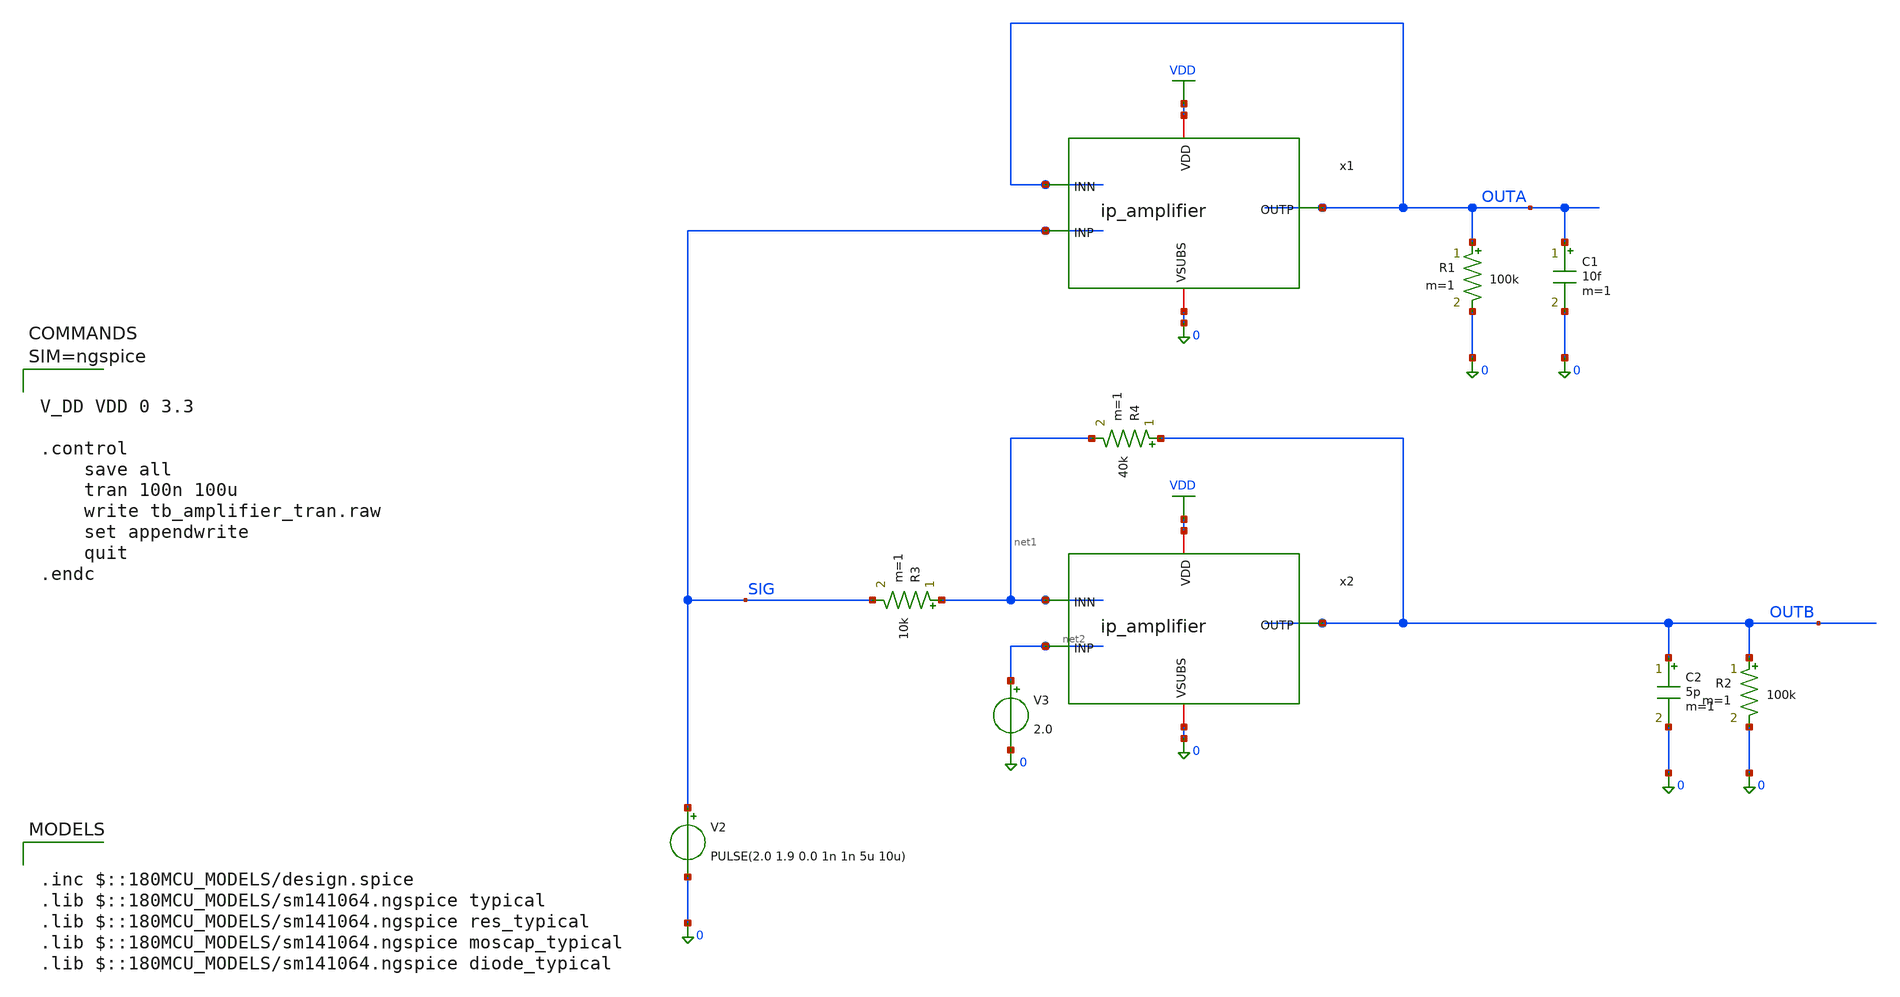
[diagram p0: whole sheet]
** sch_path: xschem/tb_amplifier_tran.sch
**.subckt tb_amplifier_tran
V2 SIG 0 PULSE(2.0 1.9 0.0 1n 1n 5u 10u)
x2 VDD OUTB net2 net1 0 ip_amplifier
R2 OUTB 0 100k m=1
C2 OUTB 0 5p m=1
V3 net2 0 2.0
R3 net1 SIG 10k m=1
R4 OUTB net1 40k m=1
x1 VDD OUTA SIG OUTA 0 ip_amplifier
R1 OUTA 0 100k m=1
C1 OUTA 0 10f m=1
**** begin user architecture code

.inc $::180MCU_MODELS/design.spice
.lib $::180MCU_MODELS/sm141064.ngspice typical
.lib $::180MCU_MODELS/sm141064.ngspice res_typical
.lib $::180MCU_MODELS/sm141064.ngspice moscap_typical
.lib $::180MCU_MODELS/sm141064.ngspice diode_typical




V_DD VDD 0 3.3

.control
	save all
	tran 100n 100u
	write tb_amplifier_tran.raw
	set appendwrite
	quit
.endc



**** end user architecture code
**.ends

* expanding   symbol:  ip_amplifier.sym # of pins=5
** sym_path: xschem/ip_amplifier.sym
** sch_path: xschem/ip_amplifier.sch
.subckt ip_amplifier VDD OUTP INP INN VSUBS
*.iopin VDD
*.iopin VSUBS
*.ipin INP
*.ipin INN
*.opin OUTP
XM1 net10 INP net8 VDD pfet_06v0 L=0.7u W=7.0u nf=1 ad='int((nf+1)/2) * W/nf * 0.18u' as='int((nf+2)/2) * W/nf * 0.18u'
+ pd='2*int((nf+1)/2) * (W/nf + 0.18u)' ps='2*int((nf+2)/2) * (W/nf + 0.18u)' nrd='0.18u / W' nrs='0.18u / W'
+ sa=0 sb=0 sd=0 m=3 par=3
XM2 net9 INN net8 VDD pfet_06v0 L=0.7u W=7.0u nf=1 ad='int((nf+1)/2) * W/nf * 0.18u' as='int((nf+2)/2) * W/nf * 0.18u'
+ pd='2*int((nf+1)/2) * (W/nf + 0.18u)' ps='2*int((nf+2)/2) * (W/nf + 0.18u)' nrd='0.18u / W' nrs='0.18u / W'
+ sa=0 sb=0 sd=0 m=3 par=3
XM5 net10 net1 VSUBS vsubs nfet_06v0 L=2u W=5u nf=1 ad='int((nf+1)/2) * W/nf * 0.18u' as='int((nf+2)/2) * W/nf * 0.18u'
+ pd='2*int((nf+1)/2) * (W/nf + 0.18u)' ps='2*int((nf+2)/2) * (W/nf + 0.18u)' nrd='0.18u / W' nrs='0.18u / W'
+ sa=0 sb=0 sd=0 m=1 par=1
XM6 net9 net1 VSUBS vsubs nfet_06v0 L=2u W=5u nf=1 ad='int((nf+1)/2) * W/nf * 0.18u' as='int((nf+2)/2) * W/nf * 0.18u'
+ pd='2*int((nf+1)/2) * (W/nf + 0.18u)' ps='2*int((nf+2)/2) * (W/nf + 0.18u)' nrd='0.18u / W' nrs='0.18u / W'
+ sa=0 sb=0 sd=0 m=1 par=1
XM3 net3 net1 VSUBS vsubs nfet_06v0 L=1u W=5u nf=1 ad='int((nf+1)/2) * W/nf * 0.18u' as='int((nf+2)/2) * W/nf * 0.18u'
+ pd='2*int((nf+1)/2) * (W/nf + 0.18u)' ps='2*int((nf+2)/2) * (W/nf + 0.18u)' nrd='0.18u / W' nrs='0.18u / W'
+ sa=0 sb=0 sd=0 m=5 par=5
XM4 net2 net1 VSUBS vsubs nfet_06v0 L=1u W=5u nf=1 ad='int((nf+1)/2) * W/nf * 0.18u' as='int((nf+2)/2) * W/nf * 0.18u'
+ pd='2*int((nf+1)/2) * (W/nf + 0.18u)' ps='2*int((nf+2)/2) * (W/nf + 0.18u)' nrd='0.18u / W' nrs='0.18u / W'
+ sa=0 sb=0 sd=0 m=1 par=1
XM7 net1 net1 net3 vsubs nfet_06v0 L=0.7u W=5u nf=1 ad='int((nf+1)/2) * W/nf * 0.18u' as='int((nf+2)/2) * W/nf * 0.18u'
+ pd='2*int((nf+1)/2) * (W/nf + 0.18u)' ps='2*int((nf+2)/2) * (W/nf + 0.18u)' nrd='0.18u / W' nrs='0.18u / W'
+ sa=0 sb=0 sd=0 m=7 par=7
XM8 net4 net1 net2 vsubs nfet_06v0 L=0.7u W=5u nf=1 ad='int((nf+1)/2) * W/nf * 0.18u' as='int((nf+2)/2) * W/nf * 0.18u'
+ pd='2*int((nf+1)/2) * (W/nf + 0.18u)' ps='2*int((nf+2)/2) * (W/nf + 0.18u)' nrd='0.18u / W' nrs='0.18u / W'
+ sa=0 sb=0 sd=0 m=7 par=7
XM9 net5 net7 VDD VDD pfet_06v0 L=1u W=6u nf=1 ad='int((nf+1)/2) * W/nf * 0.18u' as='int((nf+2)/2) * W/nf * 0.18u'
+ pd='2*int((nf+1)/2) * (W/nf + 0.18u)' ps='2*int((nf+2)/2) * (W/nf + 0.18u)' nrd='0.18u / W' nrs='0.18u / W'
+ sa=0 sb=0 sd=0 m=1 par=1
XM10 net6 net7 VDD VDD pfet_06v0 L=1u W=6u nf=1 ad='int((nf+1)/2) * W/nf * 0.18u' as='int((nf+2)/2) * W/nf * 0.18u'
+ pd='2*int((nf+1)/2) * (W/nf + 0.18u)' ps='2*int((nf+2)/2) * (W/nf + 0.18u)' nrd='0.18u / W' nrs='0.18u / W'
+ sa=0 sb=0 sd=0 m=1 par=1
XM11 net7 net7 net5 VDD pfet_06v0 L=0.7u W=7u nf=1 ad='int((nf+1)/2) * W/nf * 0.18u' as='int((nf+2)/2) * W/nf * 0.18u'
+ pd='2*int((nf+1)/2) * (W/nf + 0.18u)' ps='2*int((nf+2)/2) * (W/nf + 0.18u)' nrd='0.18u / W' nrs='0.18u / W'
+ sa=0 sb=0 sd=0 m=5 par=5
XM12 net8 net7 net6 VDD pfet_06v0 L=0.7u W=7u nf=1 ad='int((nf+1)/2) * W/nf * 0.18u' as='int((nf+2)/2) * W/nf * 0.18u'
+ pd='2*int((nf+1)/2) * (W/nf + 0.18u)' ps='2*int((nf+2)/2) * (W/nf + 0.18u)' nrd='0.18u / W' nrs='0.18u / W'
+ sa=0 sb=0 sd=0 m=5 par=5
XM13 net11 net1 net9 vsubs nfet_06v0 L=0.7u W=7u nf=1 ad='int((nf+1)/2) * W/nf * 0.18u' as='int((nf+2)/2) * W/nf * 0.18u'
+ pd='2*int((nf+1)/2) * (W/nf + 0.18u)' ps='2*int((nf+2)/2) * (W/nf + 0.18u)' nrd='0.18u / W' nrs='0.18u / W'
+ sa=0 sb=0 sd=0 m=1 par=1
XM14 net12 net1 net10 vsubs nfet_06v0 L=0.7u W=7u nf=1 ad='int((nf+1)/2) * W/nf * 0.18u' as='int((nf+2)/2) * W/nf * 0.18u'
+ pd='2*int((nf+1)/2) * (W/nf + 0.18u)' ps='2*int((nf+2)/2) * (W/nf + 0.18u)' nrd='0.18u / W' nrs='0.18u / W'
+ sa=0 sb=0 sd=0 m=1 par=1
XM15 net11 net11 VDD VDD pfet_06v0 L=0.7u W=7u nf=1 ad='int((nf+1)/2) * W/nf * 0.18u' as='int((nf+2)/2) * W/nf * 0.18u'
+ pd='2*int((nf+1)/2) * (W/nf + 0.18u)' ps='2*int((nf+2)/2) * (W/nf + 0.18u)' nrd='0.18u / W' nrs='0.18u / W'
+ sa=0 sb=0 sd=0 m=1 par=1
XM16 net12 net11 VDD VDD pfet_06v0 L=0.7u W=7u nf=1 ad='int((nf+1)/2) * W/nf * 0.18u' as='int((nf+2)/2) * W/nf * 0.18u'
+ pd='2*int((nf+1)/2) * (W/nf + 0.18u)' ps='2*int((nf+2)/2) * (W/nf + 0.18u)' nrd='0.18u / W' nrs='0.18u / W'
+ sa=0 sb=0 sd=0 m=1 par=1
XM17 OUTP net12 VDD VDD pfet_06v0 L=0.5u W=5u nf=1 ad='int((nf+1)/2) * W/nf * 0.18u' as='int((nf+2)/2) * W/nf * 0.18u'
+ pd='2*int((nf+1)/2) * (W/nf + 0.18u)' ps='2*int((nf+2)/2) * (W/nf + 0.18u)' nrd='0.18u / W' nrs='0.18u / W'
+ sa=0 sb=0 sd=0 m=12 par=12
XM18 OUTP net10 VSUBS vsubs nfet_06v0 L=0.7u W=5u nf=1 ad='int((nf+1)/2) * W/nf * 0.18u' as='int((nf+2)/2) * W/nf * 0.18u'
+ pd='2*int((nf+1)/2) * (W/nf + 0.18u)' ps='2*int((nf+2)/2) * (W/nf + 0.18u)' nrd='0.18u / W' nrs='0.18u / W'
+ sa=0 sb=0 sd=0 m=6 par=6
XR3 net1 net15 vsubs ppolyf_u_1k_6p0 r_width=1e-6 r_length=6e-6 m=1
XR6 net15 net14 vsubs ppolyf_u_1k_6p0 r_width=1e-6 r_length=6e-6 m=1
XR7 net14 net13 vsubs ppolyf_u_1k_6p0 r_width=1e-6 r_length=6e-6 m=1
XR8 net13 net16 vsubs ppolyf_u_1k_6p0 r_width=1e-6 r_length=4e-6 m=1
Vmeas VDD net16 0
Vmeas1 net7 net4 0
XC4 net17 OUTP cap_nmos_03v3 c_width=15e-6 c_length=15e-6 m=1
XC1 net18 OUTP cap_nmos_03v3 c_width=15e-6 c_length=15e-6 m=1
XC2 net19 OUTP cap_nmos_03v3 c_width=15e-6 c_length=15e-6 m=1
R9 net17 net12 15000 m=1
R10 net18 net12 15000 m=1
R11 net19 net12 15000 m=1
.ends

.GLOBAL VDD
.end
